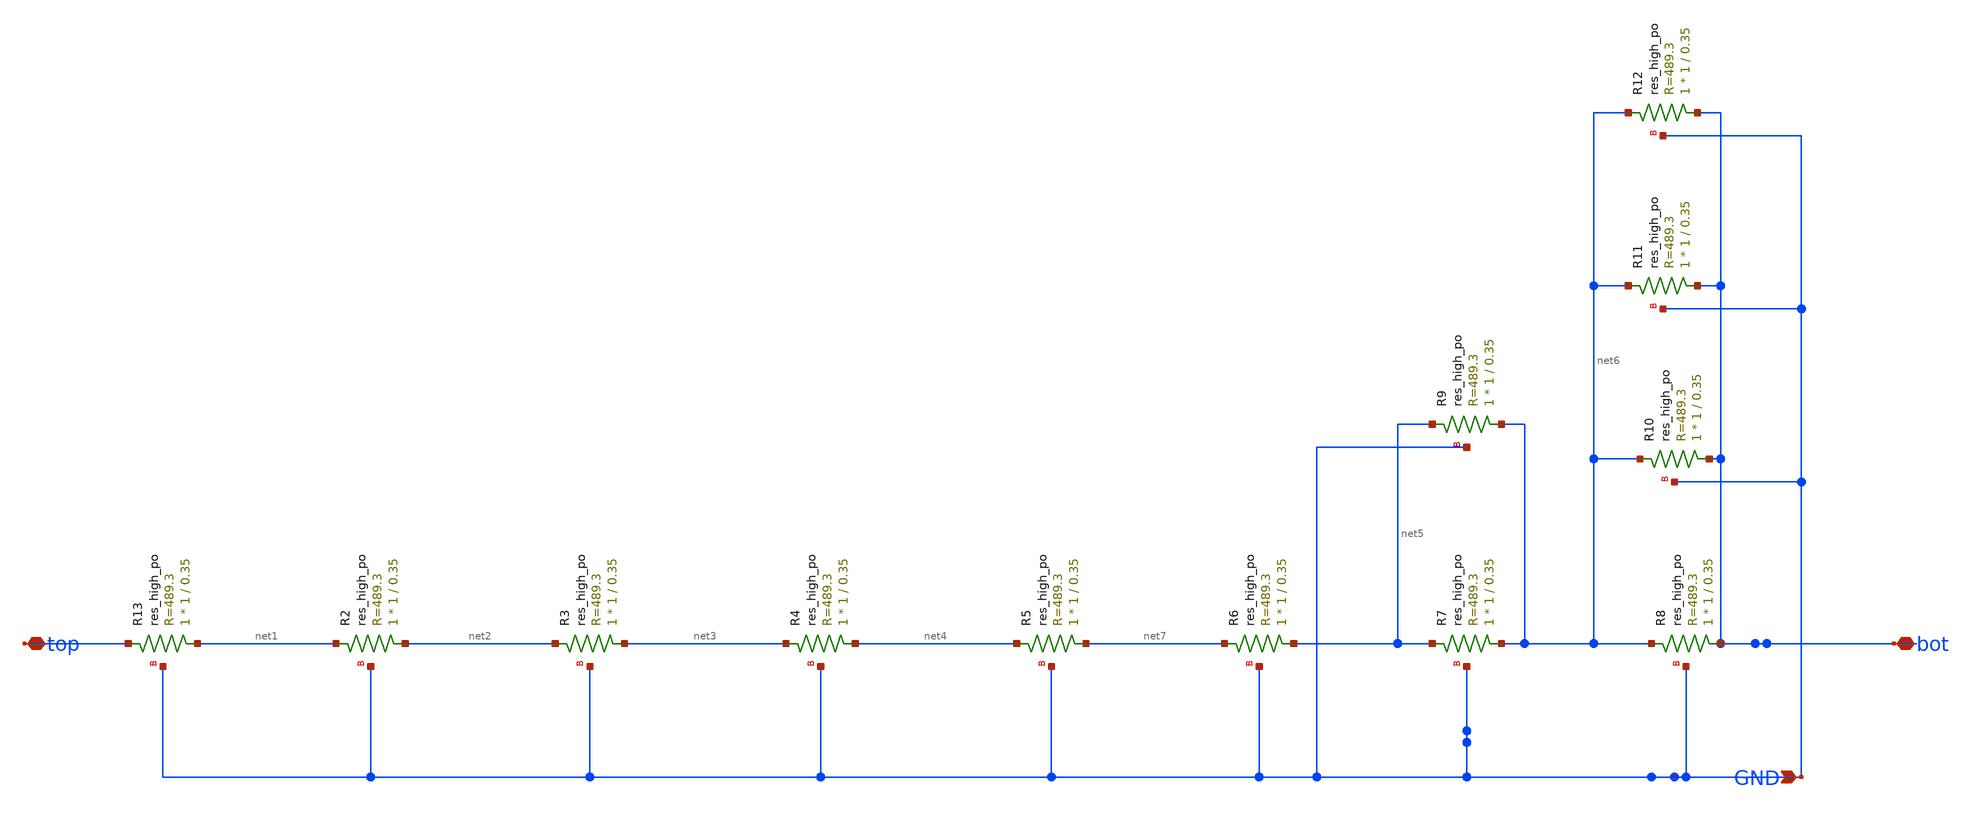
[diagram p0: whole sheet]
** sch_path: r_135k_18.sch
**.subckt r_135k_18 bot GND top
*.iopin bot
*.ipin GND
*.iopin top
XR2 net2 net1 GND sky130_fd_pr__res_high_po W=1 L=0.35 mult=1 m=1
XR3 net3 net2 GND sky130_fd_pr__res_high_po W=1 L=0.35 mult=1 m=1
XR4 net4 net3 GND sky130_fd_pr__res_high_po W=1 L=0.35 mult=1 m=1
XR5 net7 net4 GND sky130_fd_pr__res_high_po W=1 L=0.35 mult=1 m=1
XR6 net5 net7 GND sky130_fd_pr__res_high_po W=1 L=0.35 mult=1 m=1
XR7 net6 net5 GND sky130_fd_pr__res_high_po W=1 L=0.35 mult=1 m=1
XR8 bot net6 GND sky130_fd_pr__res_high_po W=1 L=0.35 mult=1 m=1
XR9 net6 net5 GND sky130_fd_pr__res_high_po W=1 L=0.35 mult=1 m=1
XR10 bot net6 GND sky130_fd_pr__res_high_po W=1 L=0.35 mult=1 m=1
XR11 bot net6 GND sky130_fd_pr__res_high_po W=1 L=0.35 mult=1 m=1
XR12 bot net6 GND sky130_fd_pr__res_high_po W=1 L=0.35 mult=1 m=1
XR13 net1 top GND sky130_fd_pr__res_high_po W=1 L=0.35 mult=1 m=1
**.ends
.end
